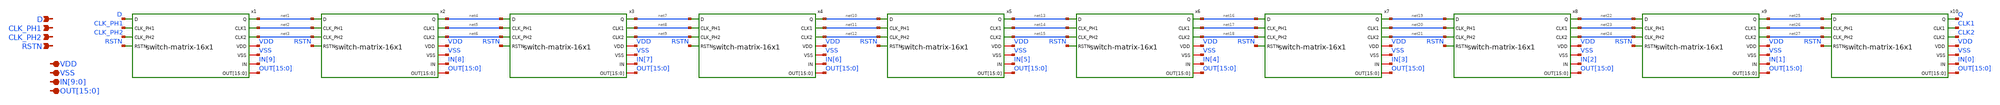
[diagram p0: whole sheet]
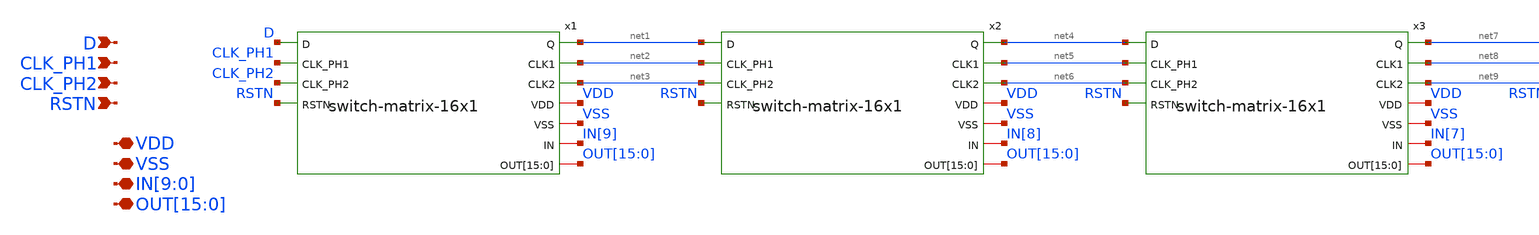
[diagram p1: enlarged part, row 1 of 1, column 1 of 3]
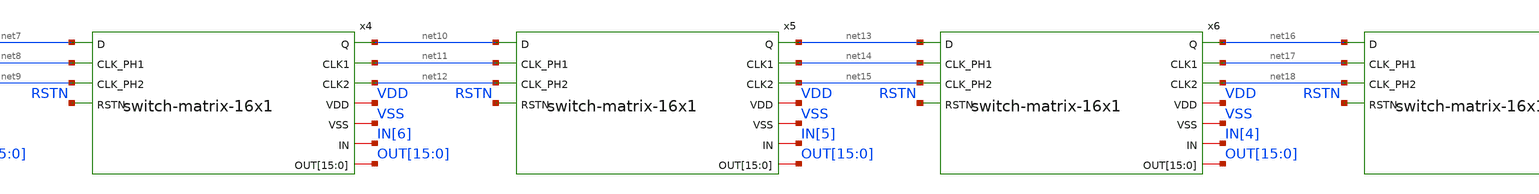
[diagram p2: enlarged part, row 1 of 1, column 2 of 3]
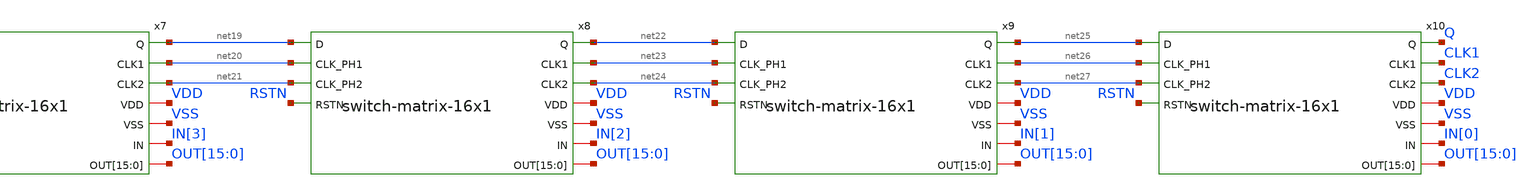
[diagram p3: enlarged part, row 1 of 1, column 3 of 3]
** sch_path: designs/libs/core_switch-matrix/switch-matrix-16x10/switch-matrix-16x10.sch
**.subckt switch-matrix-16x10 D CLK_PH1 CLK_PH2 RSTN VDD VSS
*+ IN[9],IN[8],IN[7],IN[6],IN[5],IN[4],IN[3],IN[2],IN[1],IN[0]
*+ OUT[15],OUT[14],OUT[13],OUT[12],OUT[11],OUT[10],OUT[9],OUT[8],OUT[7],OUT[6],OUT[5],OUT[4],OUT[3],OUT[2],OUT[1],OUT[0]
*.ipin D
*.ipin CLK_PH1
*.ipin CLK_PH2
*.ipin RSTN
*.iopin VDD
*.iopin VSS
*.iopin IN[9],IN[8],IN[7],IN[6],IN[5],IN[4],IN[3],IN[2],IN[1],IN[0]
*.iopin
*+ OUT[15],OUT[14],OUT[13],OUT[12],OUT[11],OUT[10],OUT[9],OUT[8],OUT[7],OUT[6],OUT[5],OUT[4],OUT[3],OUT[2],OUT[1],OUT[0]
x1 net1 net2 net3 VDD VSS IN[9] OUT[15] OUT[14] OUT[13] OUT[12] OUT[11] OUT[10] OUT[9] OUT[8] OUT[7]
+ OUT[6] OUT[5] OUT[4] OUT[3] OUT[2] OUT[1] OUT[0] D CLK_PH1 CLK_PH2 RSTN switch-matrix-16x1
x2 net4 net5 net6 VDD VSS IN[8] OUT[15] OUT[14] OUT[13] OUT[12] OUT[11] OUT[10] OUT[9] OUT[8] OUT[7]
+ OUT[6] OUT[5] OUT[4] OUT[3] OUT[2] OUT[1] OUT[0] net1 net2 net3 RSTN switch-matrix-16x1
x3 net7 net8 net9 VDD VSS IN[7] OUT[15] OUT[14] OUT[13] OUT[12] OUT[11] OUT[10] OUT[9] OUT[8] OUT[7]
+ OUT[6] OUT[5] OUT[4] OUT[3] OUT[2] OUT[1] OUT[0] net4 net5 net6 RSTN switch-matrix-16x1
x4 net10 net11 net12 VDD VSS IN[6] OUT[15] OUT[14] OUT[13] OUT[12] OUT[11] OUT[10] OUT[9] OUT[8]
+ OUT[7] OUT[6] OUT[5] OUT[4] OUT[3] OUT[2] OUT[1] OUT[0] net7 net8 net9 RSTN switch-matrix-16x1
x5 net13 net14 net15 VDD VSS IN[5] OUT[15] OUT[14] OUT[13] OUT[12] OUT[11] OUT[10] OUT[9] OUT[8]
+ OUT[7] OUT[6] OUT[5] OUT[4] OUT[3] OUT[2] OUT[1] OUT[0] net10 net11 net12 RSTN switch-matrix-16x1
x6 net16 net17 net18 VDD VSS IN[4] OUT[15] OUT[14] OUT[13] OUT[12] OUT[11] OUT[10] OUT[9] OUT[8]
+ OUT[7] OUT[6] OUT[5] OUT[4] OUT[3] OUT[2] OUT[1] OUT[0] net13 net14 net15 RSTN switch-matrix-16x1
x7 net19 net20 net21 VDD VSS IN[3] OUT[15] OUT[14] OUT[13] OUT[12] OUT[11] OUT[10] OUT[9] OUT[8]
+ OUT[7] OUT[6] OUT[5] OUT[4] OUT[3] OUT[2] OUT[1] OUT[0] net16 net17 net18 RSTN switch-matrix-16x1
x8 net22 net23 net24 VDD VSS IN[2] OUT[15] OUT[14] OUT[13] OUT[12] OUT[11] OUT[10] OUT[9] OUT[8]
+ OUT[7] OUT[6] OUT[5] OUT[4] OUT[3] OUT[2] OUT[1] OUT[0] net19 net20 net21 RSTN switch-matrix-16x1
x9 net25 net26 net27 VDD VSS IN[1] OUT[15] OUT[14] OUT[13] OUT[12] OUT[11] OUT[10] OUT[9] OUT[8]
+ OUT[7] OUT[6] OUT[5] OUT[4] OUT[3] OUT[2] OUT[1] OUT[0] net22 net23 net24 RSTN switch-matrix-16x1
x10 Q CLK1 CLK2 VDD VSS IN[0] OUT[15] OUT[14] OUT[13] OUT[12] OUT[11] OUT[10] OUT[9] OUT[8] OUT[7]
+ OUT[6] OUT[5] OUT[4] OUT[3] OUT[2] OUT[1] OUT[0] net25 net26 net27 RSTN switch-matrix-16x1
**.ends
.end
